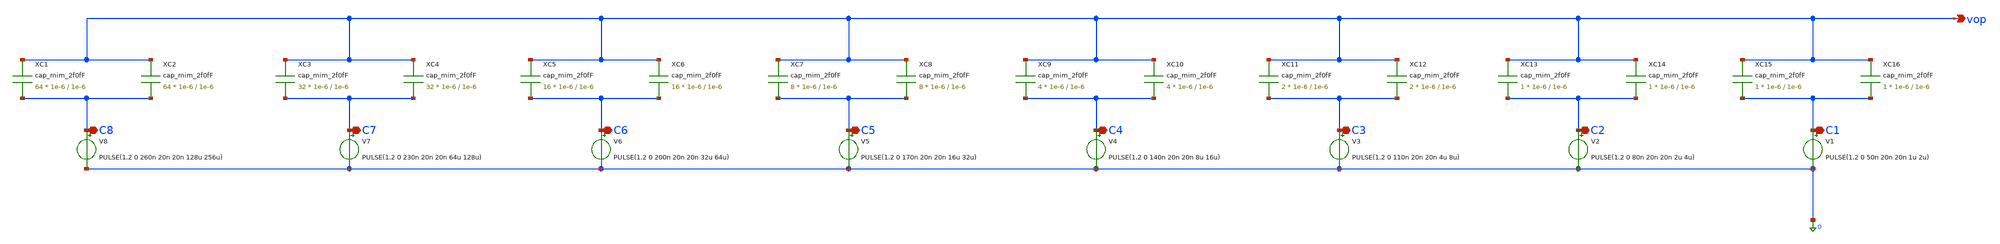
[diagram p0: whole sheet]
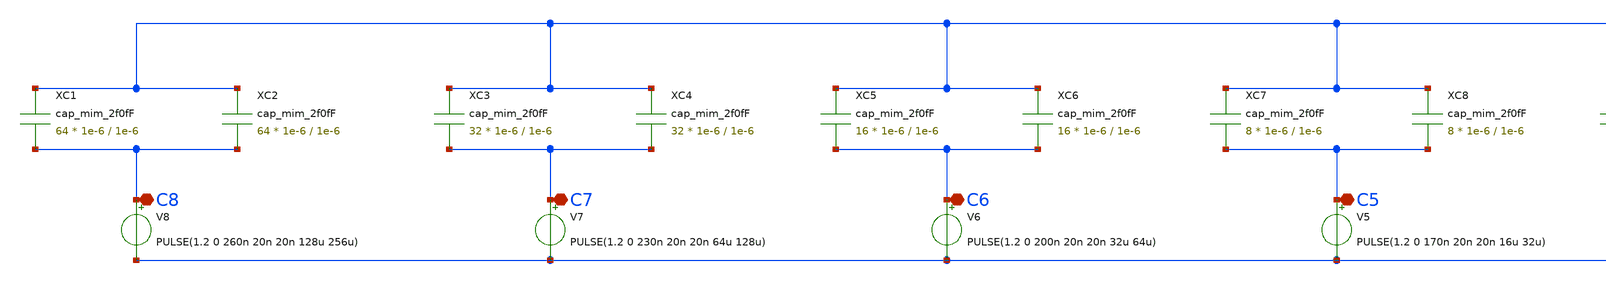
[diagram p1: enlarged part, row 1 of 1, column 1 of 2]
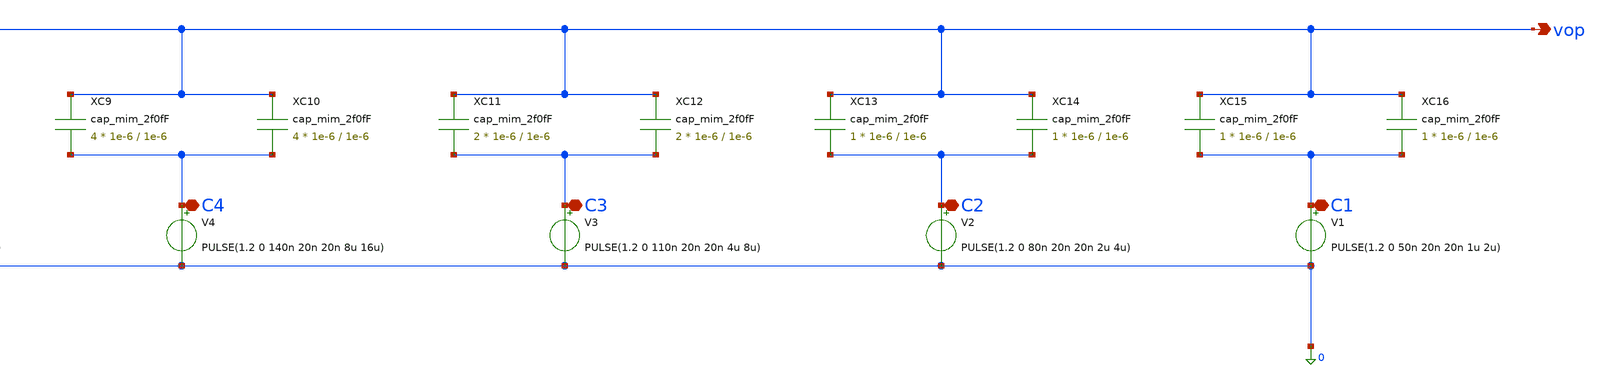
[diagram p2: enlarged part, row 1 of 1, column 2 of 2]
** sch_path: xschem/tb_CDAC.sch
**.subckt tb_CDAC C8 C7 C6 C5 C4 C3 C2 C1 vop
*.iopin C8
*.iopin C7
*.iopin C6
*.iopin C5
*.iopin C4
*.iopin C3
*.iopin C2
*.iopin C1
*.opin vop
XC1 vop C8 cap_mim_2f0fF c_width=1e-6 c_length=1e-6 m=64
XC2 vop C8 cap_mim_2f0fF c_width=1e-6 c_length=1e-6 m=64
XC3 vop C7 cap_mim_2f0fF c_width=1e-6 c_length=1e-6 m=32
XC4 vop C7 cap_mim_2f0fF c_width=1e-6 c_length=1e-6 m=32
XC5 vop C6 cap_mim_2f0fF c_width=1e-6 c_length=1e-6 m=16
XC6 vop C6 cap_mim_2f0fF c_width=1e-6 c_length=1e-6 m=16
XC7 vop C5 cap_mim_2f0fF c_width=1e-6 c_length=1e-6 m=8
XC8 vop C5 cap_mim_2f0fF c_width=1e-6 c_length=1e-6 m=8
XC9 vop C4 cap_mim_2f0fF c_width=1e-6 c_length=1e-6 m=4
XC10 vop C4 cap_mim_2f0fF c_width=1e-6 c_length=1e-6 m=4
XC11 vop C3 cap_mim_2f0fF c_width=1e-6 c_length=1e-6 m=2
XC12 vop C3 cap_mim_2f0fF c_width=1e-6 c_length=1e-6 m=2
XC13 vop C2 cap_mim_2f0fF c_width=1e-6 c_length=1e-6 m=1
XC14 vop C2 cap_mim_2f0fF c_width=1e-6 c_length=1e-6 m=1
XC15 vop C1 cap_mim_2f0fF c_width=1e-6 c_length=1e-6 m=1
XC16 vop C1 cap_mim_2f0fF c_width=1e-6 c_length=1e-6 m=1
V1 C1 0 PULSE(1.2 0 50n 20n 20n 1u 2u)
V2 C2 0 PULSE(1.2 0 80n 20n 20n 2u 4u)
V3 C3 0 PULSE(1.2 0 110n 20n 20n 4u 8u)
V4 C4 0 PULSE(1.2 0 140n 20n 20n 8u 16u)
V5 C5 0 PULSE(1.2 0 170n 20n 20n 16u 32u)
V6 C6 0 PULSE(1.2 0 200n 20n 20n 32u 64u)
V7 C7 0 PULSE(1.2 0 230n 20n 20n 64u 128u)
V8 C8 0 PULSE(1.2 0 260n 20n 20n 128u 256u)
**** begin user architecture code



.tran 1n 500u
.control
.save all
run
plot v(c1) v(c2)+2 v(c3)+4 c(c4)+6 v(c5)+8 v(c6)+10 v(c7)+12 v(c8)+14
plot v(vop)
.endc
.end




.include $::180MCU_MODELS/design.ngspice
.lib $::180MCU_MODELS/sm141064.ngspice typical
.lib $::180MCU_MODELS/sm141064.ngspice cap_mim
.lib $::180MCU_MODELS/sm141064.ngspice res_typical
.lib $::180MCU_MODELS/sm141064.ngspice moscap_typical
.lib $::180MCU_MODELS/sm141064.ngspice mimcap_typical
* .lib $::180MCU_MODELS/sm141064.ngspice res_statistical

**** end user architecture code
**.ends
.end
